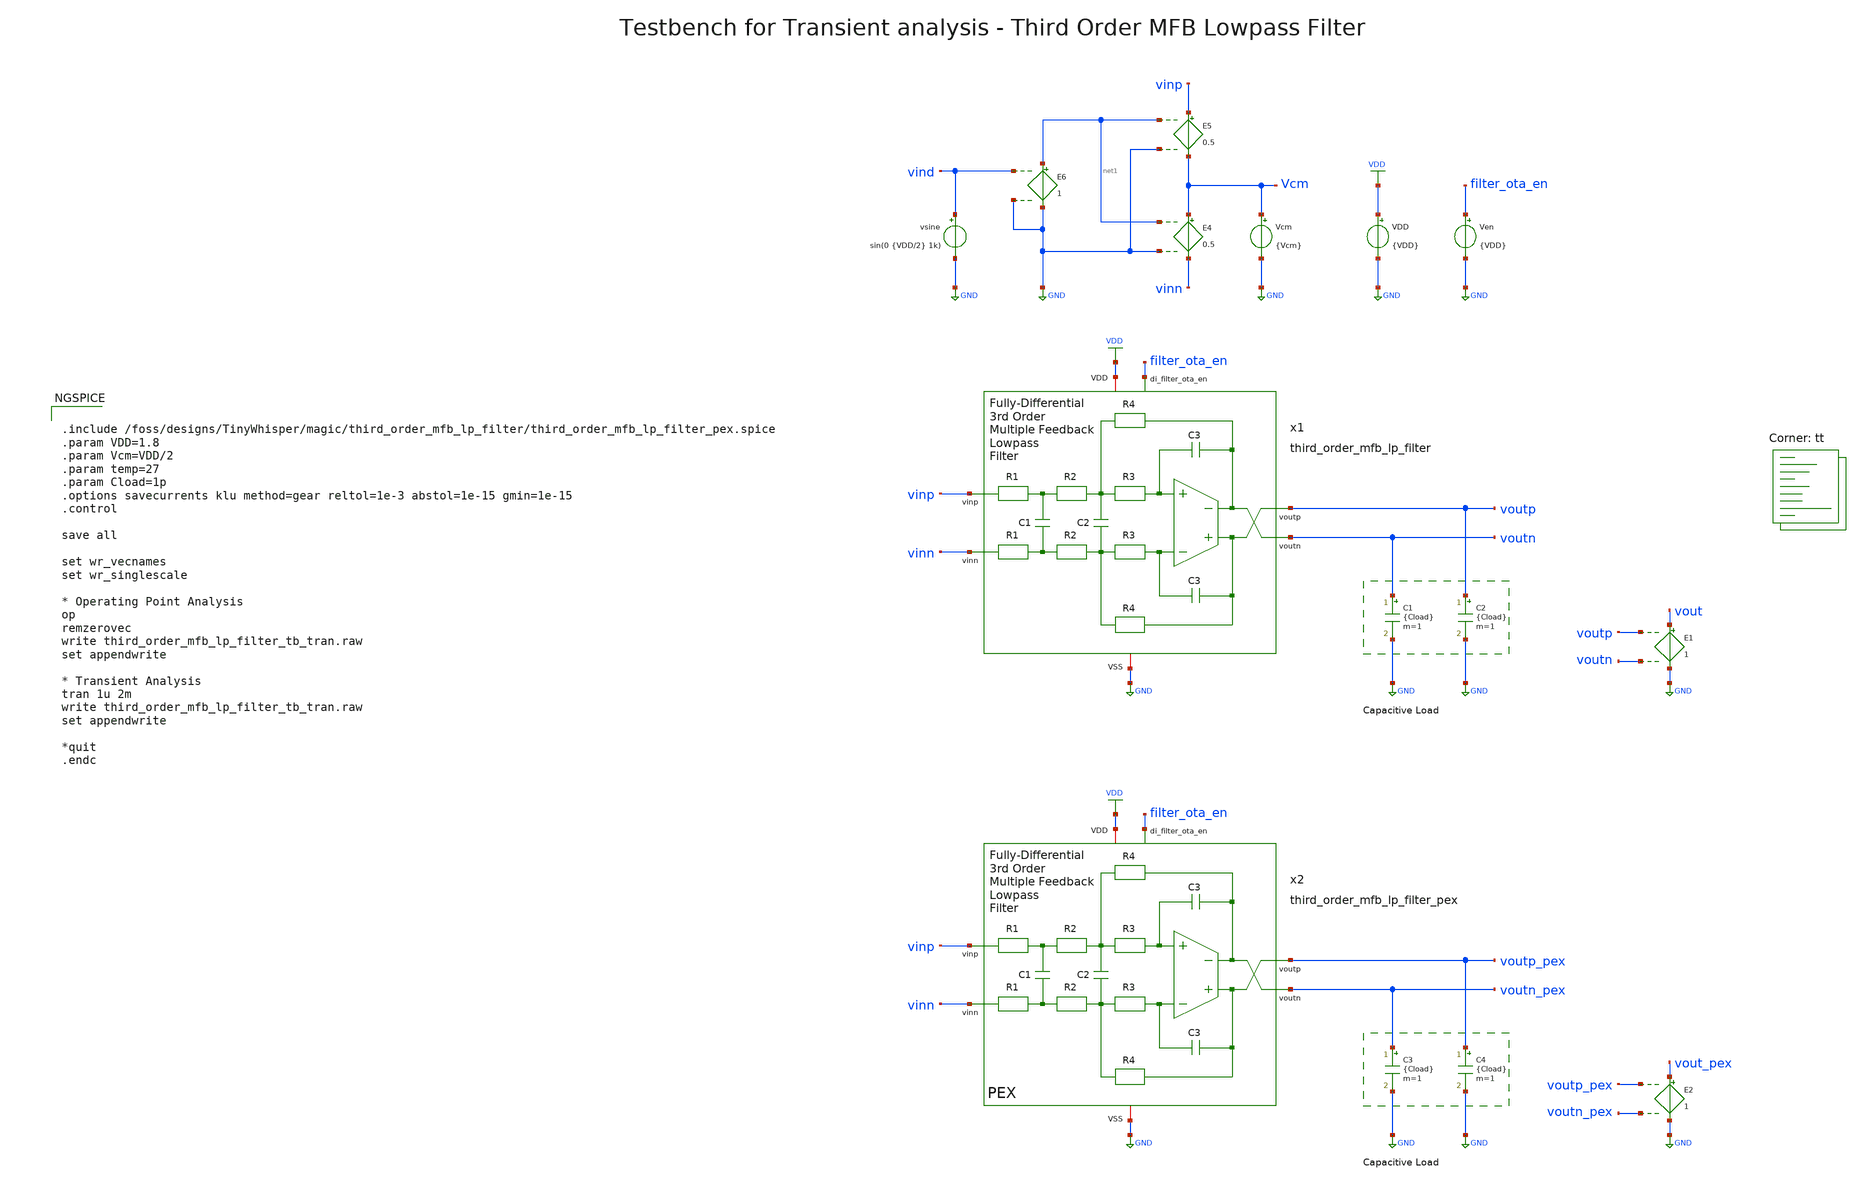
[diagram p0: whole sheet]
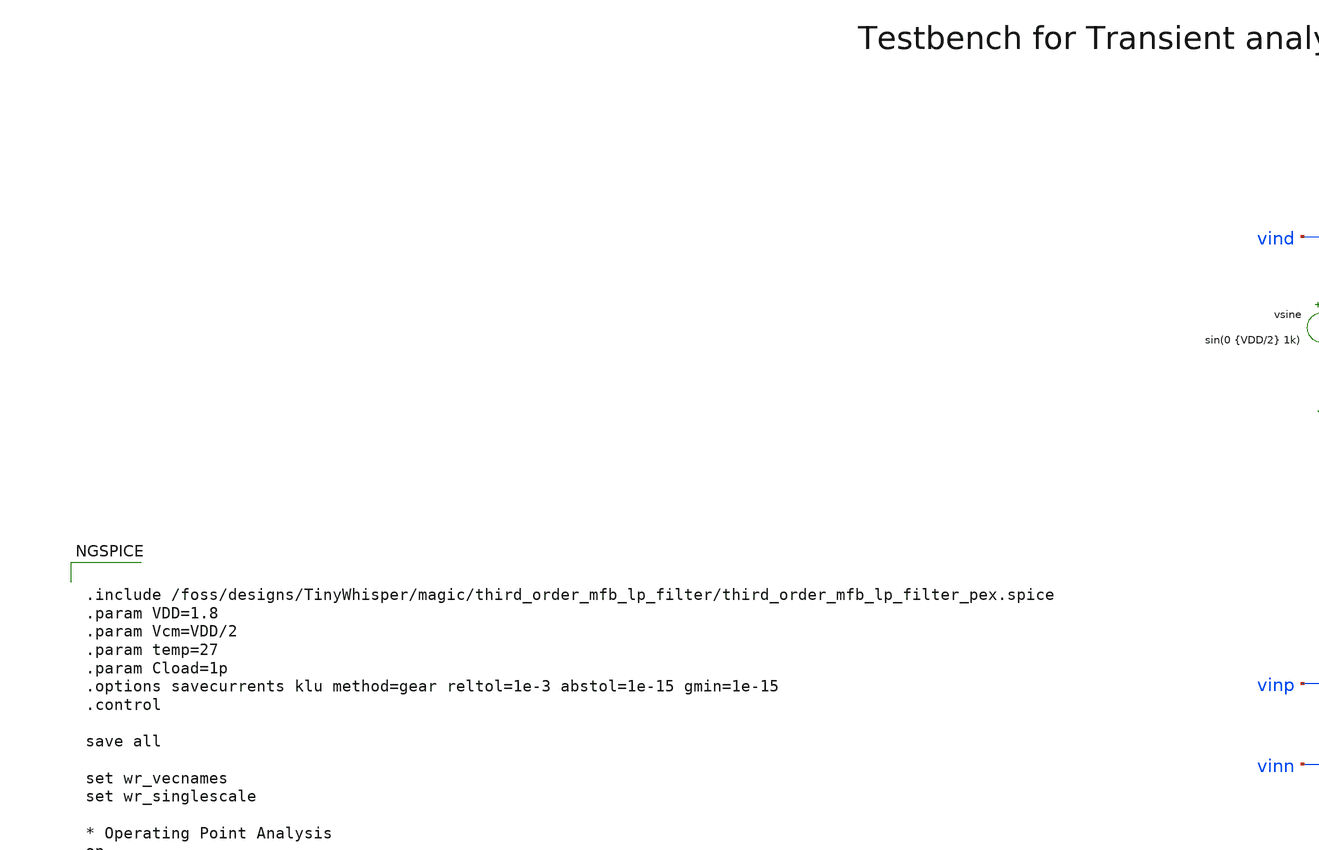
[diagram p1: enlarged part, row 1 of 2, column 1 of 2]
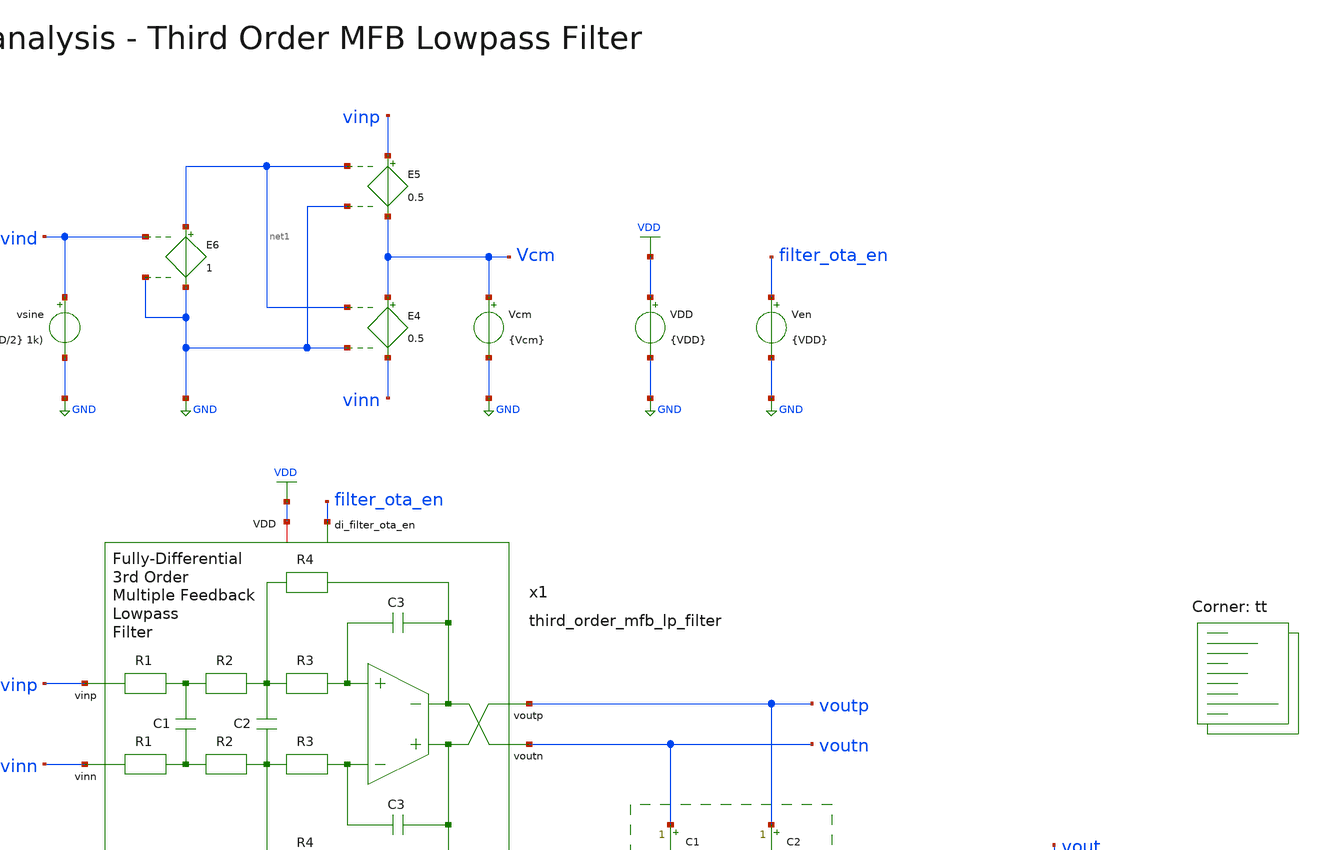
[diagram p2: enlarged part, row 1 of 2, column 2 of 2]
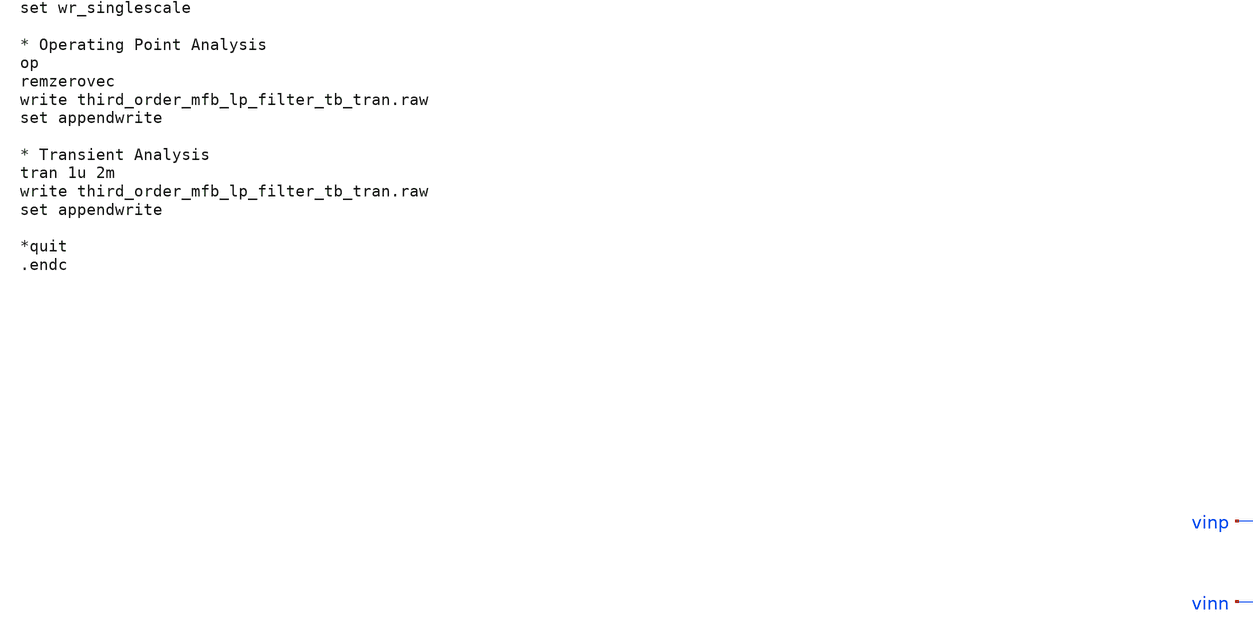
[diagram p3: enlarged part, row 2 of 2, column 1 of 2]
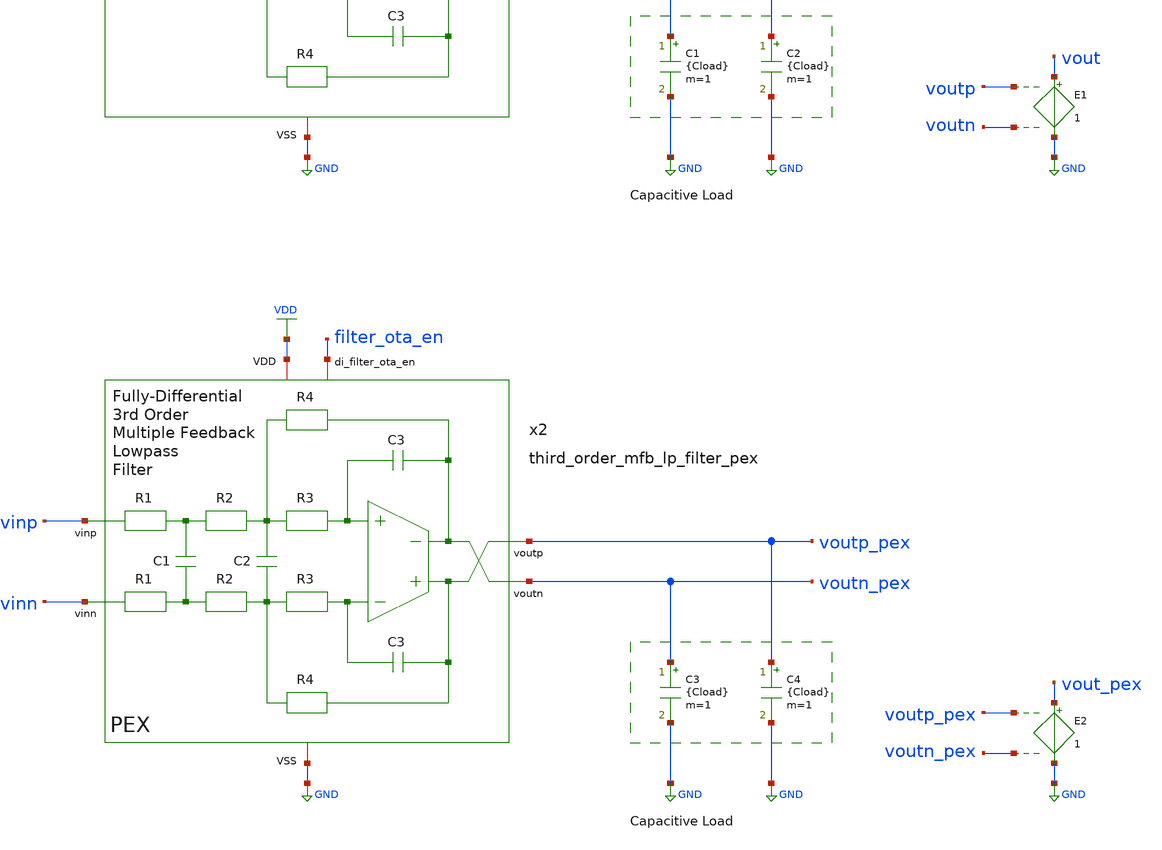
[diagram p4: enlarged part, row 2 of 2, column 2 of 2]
** sch_path: magic/iq_modulator/third_order_mfb_lp_filter/third_order_mfb_lp_filter_tb_tran.sch
**.subckt third_order_mfb_lp_filter_tb_tran
VDD VDD GND {VDD}
C1 voutn GND {Cload} m=1
C2 voutp GND {Cload} m=1
Vcm Vcm GND {Vcm}
E4 Vcm vinn net1 GND 0.5
E5 vinp Vcm net1 GND 0.5
E6 net1 GND vind GND 1
Ven filter_ota_en GND {VDD}
E1 vout GND voutp voutn 1
C3 voutn_pex GND {Cload} m=1
C4 voutp_pex GND {Cload} m=1
E2 vout_pex GND voutp_pex voutn_pex 1
vsine vind GND sin(0 {VDD/2} 1k)
x1 filter_ota_en voutp vinp voutn vinn VDD GND third_order_mfb_lp_filter
x2 filter_ota_en voutp_pex vinp voutn_pex vinn VDD GND third_order_mfb_lp_filter_pex
**** begin user architecture code


.include /foss/designs/TinyWhisper/magic/third_order_mfb_lp_filter/third_order_mfb_lp_filter_pex.spice
.param VDD=1.8
.param Vcm=VDD/2
.param temp=27
.param Cload=1p
.options savecurrents klu method=gear reltol=1e-3 abstol=1e-15 gmin=1e-15
.control

save all

set wr_vecnames
set wr_singlescale

* Operating Point Analysis
op
remzerovec
write third_order_mfb_lp_filter_tb_tran.raw
set appendwrite

* Transient Analysis
tran 1u 2m
write third_order_mfb_lp_filter_tb_tran.raw
set appendwrite

*quit
.endc


.lib $::SKYWATER_MODELS/sky130.lib.spice tt
**** end user architecture code
**.ends
.GLOBAL GND
.GLOBAL VDD
.end
